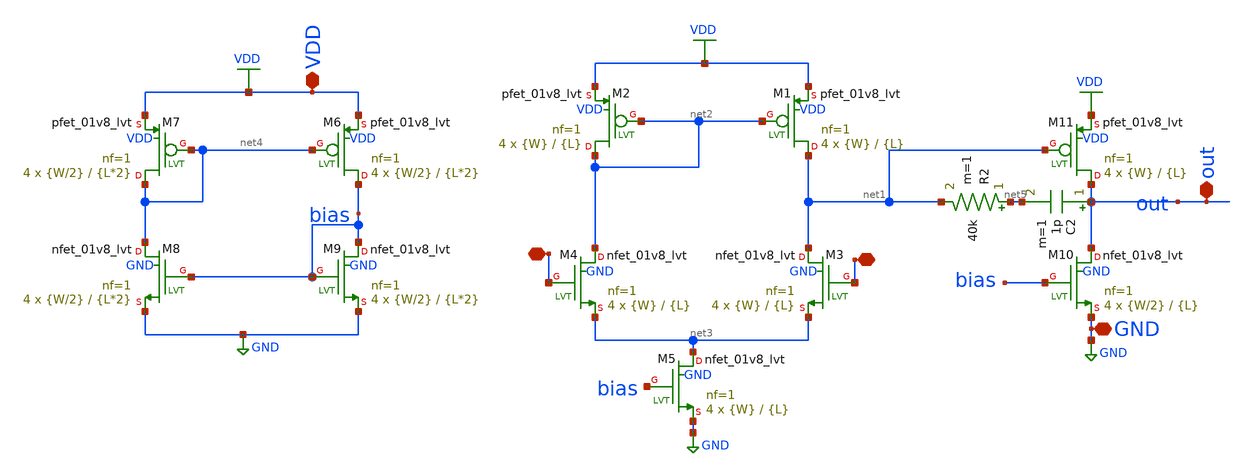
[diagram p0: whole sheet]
** sch_path: xschem/op.sch
**.subckt op VDD GND - + out
*.iopin VDD
*.iopin GND
*.iopin -
*.iopin +
*.iopin out
XM1 net1 net2 VDD VDD sky130_fd_pr__pfet_01v8_lvt L={L} W={W} nf=1 ad='int((nf+1)/2) * W/nf * 0.29' as='int((nf+2)/2) * W/nf * 0.29'
+ pd='2*int((nf+1)/2) * (W/nf + 0.29)' ps='2*int((nf+2)/2) * (W/nf + 0.29)' nrd='0.29 / W' nrs='0.29 / W'
+ sa=0 sb=0 sd=0 mult=4 m=4
XM2 net2 net2 VDD VDD sky130_fd_pr__pfet_01v8_lvt L={L} W={W} nf=1 ad='int((nf+1)/2) * W/nf * 0.29' as='int((nf+2)/2) * W/nf * 0.29'
+ pd='2*int((nf+1)/2) * (W/nf + 0.29)' ps='2*int((nf+2)/2) * (W/nf + 0.29)' nrd='0.29 / W' nrs='0.29 / W'
+ sa=0 sb=0 sd=0 mult=4 m=4
XM3 net1 + net3 GND sky130_fd_pr__nfet_01v8_lvt L={L} W={W} nf=1 ad='int((nf+1)/2) * W/nf * 0.29' as='int((nf+2)/2) * W/nf * 0.29'
+ pd='2*int((nf+1)/2) * (W/nf + 0.29)' ps='2*int((nf+2)/2) * (W/nf + 0.29)' nrd='0.29 / W' nrs='0.29 / W'
+ sa=0 sb=0 sd=0 mult=4 m=4
XM4 net2 - net3 GND sky130_fd_pr__nfet_01v8_lvt L={L} W={W} nf=1 ad='int((nf+1)/2) * W/nf * 0.29' as='int((nf+2)/2) * W/nf * 0.29'
+ pd='2*int((nf+1)/2) * (W/nf + 0.29)' ps='2*int((nf+2)/2) * (W/nf + 0.29)' nrd='0.29 / W' nrs='0.29 / W'
+ sa=0 sb=0 sd=0 mult=4 m=4
XM5 net3 bias GND GND sky130_fd_pr__nfet_01v8_lvt L={L} W={W} nf=1 ad='int((nf+1)/2) * W/nf * 0.29' as='int((nf+2)/2) * W/nf * 0.29'
+ pd='2*int((nf+1)/2) * (W/nf + 0.29)' ps='2*int((nf+2)/2) * (W/nf + 0.29)' nrd='0.29 / W' nrs='0.29 / W'
+ sa=0 sb=0 sd=0 mult=4 m=4
XM6 bias net4 VDD VDD sky130_fd_pr__pfet_01v8_lvt L={L*2} W={W/2} nf=1 ad='int((nf+1)/2) * W/nf * 0.29'
+ as='int((nf+2)/2) * W/nf * 0.29' pd='2*int((nf+1)/2) * (W/nf + 0.29)' ps='2*int((nf+2)/2) * (W/nf + 0.29)'
+ nrd='0.29 / W' nrs='0.29 / W' sa=0 sb=0 sd=0 mult=4 m=4
XM7 net4 net4 VDD VDD sky130_fd_pr__pfet_01v8_lvt L={L*2} W={W/2} nf=1 ad='int((nf+1)/2) * W/nf * 0.29'
+ as='int((nf+2)/2) * W/nf * 0.29' pd='2*int((nf+1)/2) * (W/nf + 0.29)' ps='2*int((nf+2)/2) * (W/nf + 0.29)'
+ nrd='0.29 / W' nrs='0.29 / W' sa=0 sb=0 sd=0 mult=4 m=4
XM8 net4 bias GND GND sky130_fd_pr__nfet_01v8_lvt L={L*2} W={W/2} nf=1 ad='int((nf+1)/2) * W/nf * 0.29'
+ as='int((nf+2)/2) * W/nf * 0.29' pd='2*int((nf+1)/2) * (W/nf + 0.29)' ps='2*int((nf+2)/2) * (W/nf + 0.29)'
+ nrd='0.29 / W' nrs='0.29 / W' sa=0 sb=0 sd=0 mult=4 m=4
XM9 bias bias GND GND sky130_fd_pr__nfet_01v8_lvt L={L*2} W={W/2} nf=1 ad='int((nf+1)/2) * W/nf * 0.29'
+ as='int((nf+2)/2) * W/nf * 0.29' pd='2*int((nf+1)/2) * (W/nf + 0.29)' ps='2*int((nf+2)/2) * (W/nf + 0.29)'
+ nrd='0.29 / W' nrs='0.29 / W' sa=0 sb=0 sd=0 mult=4 m=4
XM10 out bias GND GND sky130_fd_pr__nfet_01v8_lvt L={L} W={W/2} nf=1 ad='int((nf+1)/2) * W/nf * 0.29'
+ as='int((nf+2)/2) * W/nf * 0.29' pd='2*int((nf+1)/2) * (W/nf + 0.29)' ps='2*int((nf+2)/2) * (W/nf + 0.29)'
+ nrd='0.29 / W' nrs='0.29 / W' sa=0 sb=0 sd=0 mult=4 m=4
XM11 out net1 VDD VDD sky130_fd_pr__pfet_01v8_lvt L={L} W={W} nf=1 ad='int((nf+1)/2) * W/nf * 0.29' as='int((nf+2)/2) * W/nf * 0.29'
+ pd='2*int((nf+1)/2) * (W/nf + 0.29)' ps='2*int((nf+2)/2) * (W/nf + 0.29)' nrd='0.29 / W' nrs='0.29 / W'
+ sa=0 sb=0 sd=0 mult=4 m=4
C2 out net5 1p m=1
R2 net5 net1 40k m=1
**** begin user architecture code


.param L=2.7
.param W=1.5


**** end user architecture code
**.ends
.GLOBAL VDD
.GLOBAL GND
.end
